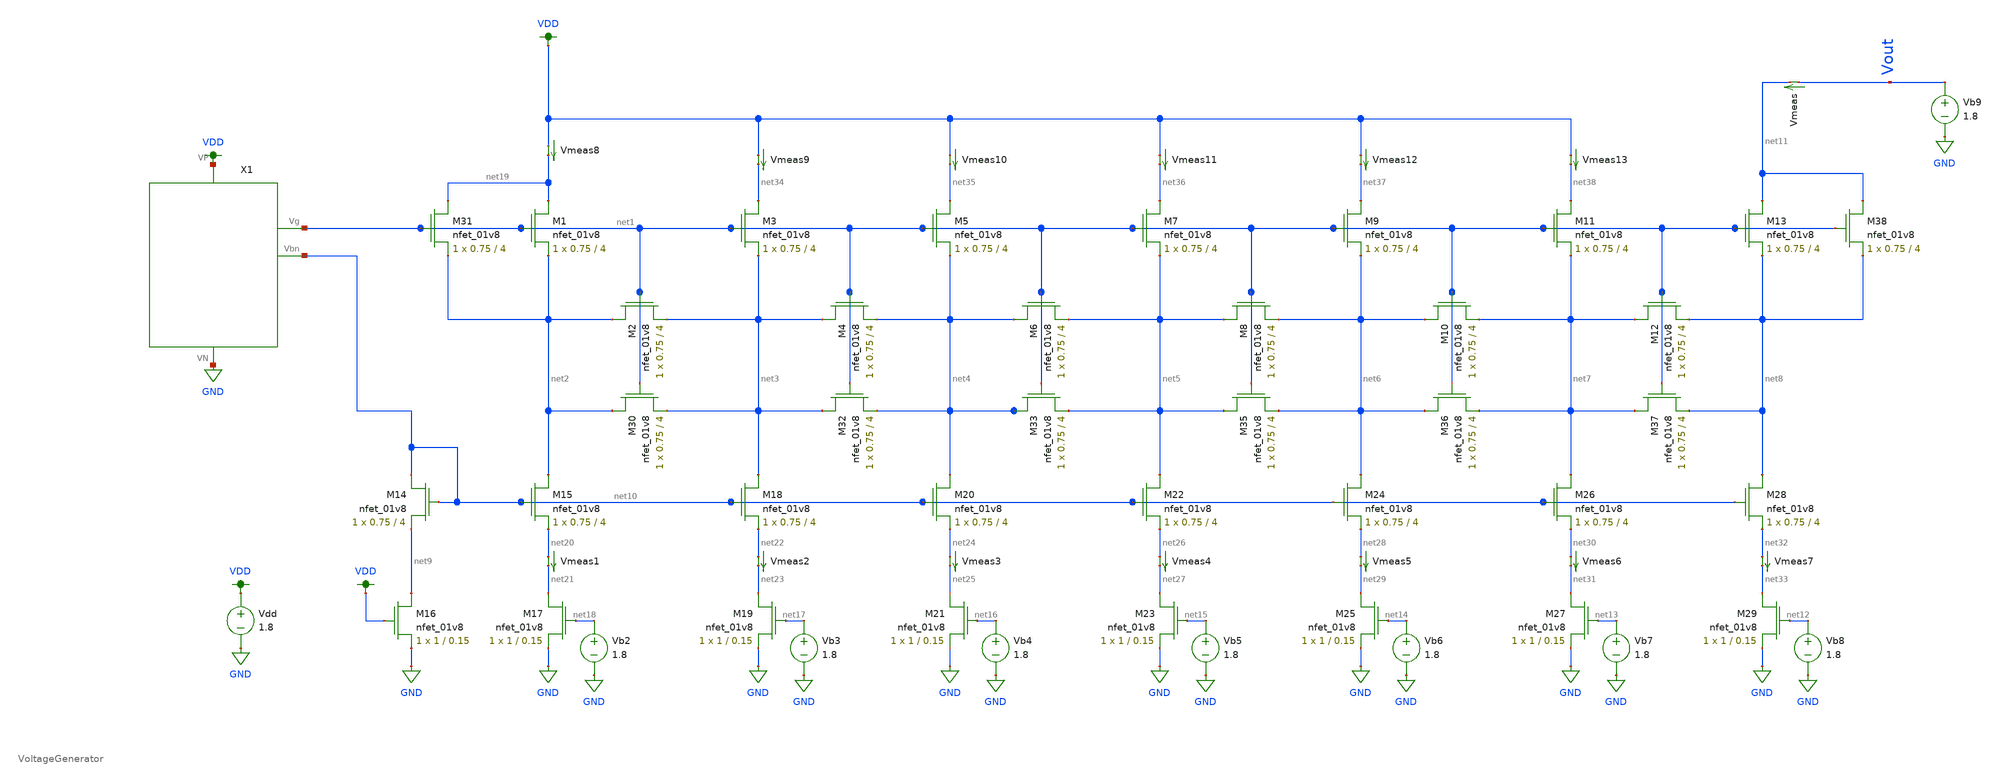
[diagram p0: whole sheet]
** sch_path: DAC_sch_test.sch
**.subckt DAC_sch_test
XM1 net19 net1 net2 GND sky130_fd_pr__nfet_01v8 L=4 W=0.75 nf=1 ad='int((nf+1)/2) * W/nf * 0.29' as='int((nf+2)/2) * W/nf * 0.29'
+ pd='2*int((nf+1)/2) * (W/nf + 0.29)' ps='2*int((nf+2)/2) * (W/nf + 0.29)' nrd='0.29 / W' nrs='0.29 / W'
+ sa=0 sb=0 sd=0 mult=1 m=1
XM2 net2 net1 net3 GND sky130_fd_pr__nfet_01v8 L=4 W=0.75 nf=1 ad='int((nf+1)/2) * W/nf * 0.29' as='int((nf+2)/2) * W/nf * 0.29'
+ pd='2*int((nf+1)/2) * (W/nf + 0.29)' ps='2*int((nf+2)/2) * (W/nf + 0.29)' nrd='0.29 / W' nrs='0.29 / W'
+ sa=0 sb=0 sd=0 mult=1 m=1
XM3 net34 net1 net3 GND sky130_fd_pr__nfet_01v8 L=4 W=0.75 nf=1 ad='int((nf+1)/2) * W/nf * 0.29' as='int((nf+2)/2) * W/nf * 0.29'
+ pd='2*int((nf+1)/2) * (W/nf + 0.29)' ps='2*int((nf+2)/2) * (W/nf + 0.29)' nrd='0.29 / W' nrs='0.29 / W'
+ sa=0 sb=0 sd=0 mult=1 m=1
XM4 net3 net1 net4 GND sky130_fd_pr__nfet_01v8 L=4 W=0.75 nf=1 ad='int((nf+1)/2) * W/nf * 0.29' as='int((nf+2)/2) * W/nf * 0.29'
+ pd='2*int((nf+1)/2) * (W/nf + 0.29)' ps='2*int((nf+2)/2) * (W/nf + 0.29)' nrd='0.29 / W' nrs='0.29 / W'
+ sa=0 sb=0 sd=0 mult=1 m=1
XM5 net35 net1 net4 GND sky130_fd_pr__nfet_01v8 L=4 W=0.75 nf=1 ad='int((nf+1)/2) * W/nf * 0.29' as='int((nf+2)/2) * W/nf * 0.29'
+ pd='2*int((nf+1)/2) * (W/nf + 0.29)' ps='2*int((nf+2)/2) * (W/nf + 0.29)' nrd='0.29 / W' nrs='0.29 / W'
+ sa=0 sb=0 sd=0 mult=1 m=1
XM6 net4 net1 net5 GND sky130_fd_pr__nfet_01v8 L=4 W=0.75 nf=1 ad='int((nf+1)/2) * W/nf * 0.29' as='int((nf+2)/2) * W/nf * 0.29'
+ pd='2*int((nf+1)/2) * (W/nf + 0.29)' ps='2*int((nf+2)/2) * (W/nf + 0.29)' nrd='0.29 / W' nrs='0.29 / W'
+ sa=0 sb=0 sd=0 mult=1 m=1
XM7 net36 net1 net5 GND sky130_fd_pr__nfet_01v8 L=4 W=0.75 nf=1 ad='int((nf+1)/2) * W/nf * 0.29' as='int((nf+2)/2) * W/nf * 0.29'
+ pd='2*int((nf+1)/2) * (W/nf + 0.29)' ps='2*int((nf+2)/2) * (W/nf + 0.29)' nrd='0.29 / W' nrs='0.29 / W'
+ sa=0 sb=0 sd=0 mult=1 m=1
XM8 net5 net1 net6 GND sky130_fd_pr__nfet_01v8 L=4 W=0.75 nf=1 ad='int((nf+1)/2) * W/nf * 0.29' as='int((nf+2)/2) * W/nf * 0.29'
+ pd='2*int((nf+1)/2) * (W/nf + 0.29)' ps='2*int((nf+2)/2) * (W/nf + 0.29)' nrd='0.29 / W' nrs='0.29 / W'
+ sa=0 sb=0 sd=0 mult=1 m=1
XM9 net37 net1 net6 GND sky130_fd_pr__nfet_01v8 L=4 W=0.75 nf=1 ad='int((nf+1)/2) * W/nf * 0.29' as='int((nf+2)/2) * W/nf * 0.29'
+ pd='2*int((nf+1)/2) * (W/nf + 0.29)' ps='2*int((nf+2)/2) * (W/nf + 0.29)' nrd='0.29 / W' nrs='0.29 / W'
+ sa=0 sb=0 sd=0 mult=1 m=1
XM10 net6 net1 net7 GND sky130_fd_pr__nfet_01v8 L=4 W=0.75 nf=1 ad='int((nf+1)/2) * W/nf * 0.29' as='int((nf+2)/2) * W/nf * 0.29'
+ pd='2*int((nf+1)/2) * (W/nf + 0.29)' ps='2*int((nf+2)/2) * (W/nf + 0.29)' nrd='0.29 / W' nrs='0.29 / W'
+ sa=0 sb=0 sd=0 mult=1 m=1
XM11 net38 net1 net7 GND sky130_fd_pr__nfet_01v8 L=4 W=0.75 nf=1 ad='int((nf+1)/2) * W/nf * 0.29' as='int((nf+2)/2) * W/nf * 0.29'
+ pd='2*int((nf+1)/2) * (W/nf + 0.29)' ps='2*int((nf+2)/2) * (W/nf + 0.29)' nrd='0.29 / W' nrs='0.29 / W'
+ sa=0 sb=0 sd=0 mult=1 m=1
XM12 net7 net1 net8 GND sky130_fd_pr__nfet_01v8 L=4 W=0.75 nf=1 ad='int((nf+1)/2) * W/nf * 0.29' as='int((nf+2)/2) * W/nf * 0.29'
+ pd='2*int((nf+1)/2) * (W/nf + 0.29)' ps='2*int((nf+2)/2) * (W/nf + 0.29)' nrd='0.29 / W' nrs='0.29 / W'
+ sa=0 sb=0 sd=0 mult=1 m=1
XM13 net11 net1 net8 GND sky130_fd_pr__nfet_01v8 L=4 W=0.75 nf=1 ad='int((nf+1)/2) * W/nf * 0.29' as='int((nf+2)/2) * W/nf * 0.29'
+ pd='2*int((nf+1)/2) * (W/nf + 0.29)' ps='2*int((nf+2)/2) * (W/nf + 0.29)' nrd='0.29 / W' nrs='0.29 / W'
+ sa=0 sb=0 sd=0 mult=1 m=1
XM14 net10 net10 net9 GND sky130_fd_pr__nfet_01v8 L=4 W=0.75 nf=1 ad='int((nf+1)/2) * W/nf * 0.29' as='int((nf+2)/2) * W/nf * 0.29'
+ pd='2*int((nf+1)/2) * (W/nf + 0.29)' ps='2*int((nf+2)/2) * (W/nf + 0.29)' nrd='0.29 / W' nrs='0.29 / W'
+ sa=0 sb=0 sd=0 mult=1 m=1
XM15 net2 net10 net20 GND sky130_fd_pr__nfet_01v8 L=4 W=0.75 nf=1 ad='int((nf+1)/2) * W/nf * 0.29' as='int((nf+2)/2) * W/nf * 0.29'
+ pd='2*int((nf+1)/2) * (W/nf + 0.29)' ps='2*int((nf+2)/2) * (W/nf + 0.29)' nrd='0.29 / W' nrs='0.29 / W'
+ sa=0 sb=0 sd=0 mult=1 m=1
XM16 net9 VDD GND GND sky130_fd_pr__nfet_01v8 L=0.15 W=1 nf=1 ad='int((nf+1)/2) * W/nf * 0.29' as='int((nf+2)/2) * W/nf * 0.29'
+ pd='2*int((nf+1)/2) * (W/nf + 0.29)' ps='2*int((nf+2)/2) * (W/nf + 0.29)' nrd='0.29 / W' nrs='0.29 / W'
+ sa=0 sb=0 sd=0 mult=1 m=1
XM17 net21 net18 GND GND sky130_fd_pr__nfet_01v8 L=0.15 W=1 nf=1 ad='int((nf+1)/2) * W/nf * 0.29' as='int((nf+2)/2) * W/nf * 0.29'
+ pd='2*int((nf+1)/2) * (W/nf + 0.29)' ps='2*int((nf+2)/2) * (W/nf + 0.29)' nrd='0.29 / W' nrs='0.29 / W'
+ sa=0 sb=0 sd=0 mult=1 m=1
XM18 net3 net10 net22 GND sky130_fd_pr__nfet_01v8 L=4 W=0.75 nf=1 ad='int((nf+1)/2) * W/nf * 0.29' as='int((nf+2)/2) * W/nf * 0.29'
+ pd='2*int((nf+1)/2) * (W/nf + 0.29)' ps='2*int((nf+2)/2) * (W/nf + 0.29)' nrd='0.29 / W' nrs='0.29 / W'
+ sa=0 sb=0 sd=0 mult=1 m=1
XM19 net23 net17 GND GND sky130_fd_pr__nfet_01v8 L=0.15 W=1 nf=1 ad='int((nf+1)/2) * W/nf * 0.29' as='int((nf+2)/2) * W/nf * 0.29'
+ pd='2*int((nf+1)/2) * (W/nf + 0.29)' ps='2*int((nf+2)/2) * (W/nf + 0.29)' nrd='0.29 / W' nrs='0.29 / W'
+ sa=0 sb=0 sd=0 mult=1 m=1
XM20 net4 net10 net24 GND sky130_fd_pr__nfet_01v8 L=4 W=0.75 nf=1 ad='int((nf+1)/2) * W/nf * 0.29' as='int((nf+2)/2) * W/nf * 0.29'
+ pd='2*int((nf+1)/2) * (W/nf + 0.29)' ps='2*int((nf+2)/2) * (W/nf + 0.29)' nrd='0.29 / W' nrs='0.29 / W'
+ sa=0 sb=0 sd=0 mult=1 m=1
XM21 net25 net16 GND GND sky130_fd_pr__nfet_01v8 L=0.15 W=1 nf=1 ad='int((nf+1)/2) * W/nf * 0.29' as='int((nf+2)/2) * W/nf * 0.29'
+ pd='2*int((nf+1)/2) * (W/nf + 0.29)' ps='2*int((nf+2)/2) * (W/nf + 0.29)' nrd='0.29 / W' nrs='0.29 / W'
+ sa=0 sb=0 sd=0 mult=1 m=1
XM22 net5 net10 net26 GND sky130_fd_pr__nfet_01v8 L=4 W=0.75 nf=1 ad='int((nf+1)/2) * W/nf * 0.29' as='int((nf+2)/2) * W/nf * 0.29'
+ pd='2*int((nf+1)/2) * (W/nf + 0.29)' ps='2*int((nf+2)/2) * (W/nf + 0.29)' nrd='0.29 / W' nrs='0.29 / W'
+ sa=0 sb=0 sd=0 mult=1 m=1
XM23 net27 net15 GND GND sky130_fd_pr__nfet_01v8 L=0.15 W=1 nf=1 ad='int((nf+1)/2) * W/nf * 0.29' as='int((nf+2)/2) * W/nf * 0.29'
+ pd='2*int((nf+1)/2) * (W/nf + 0.29)' ps='2*int((nf+2)/2) * (W/nf + 0.29)' nrd='0.29 / W' nrs='0.29 / W'
+ sa=0 sb=0 sd=0 mult=1 m=1
XM24 net6 net10 net28 GND sky130_fd_pr__nfet_01v8 L=4 W=0.75 nf=1 ad='int((nf+1)/2) * W/nf * 0.29' as='int((nf+2)/2) * W/nf * 0.29'
+ pd='2*int((nf+1)/2) * (W/nf + 0.29)' ps='2*int((nf+2)/2) * (W/nf + 0.29)' nrd='0.29 / W' nrs='0.29 / W'
+ sa=0 sb=0 sd=0 mult=1 m=1
XM25 net29 net14 GND GND sky130_fd_pr__nfet_01v8 L=0.15 W=1 nf=1 ad='int((nf+1)/2) * W/nf * 0.29' as='int((nf+2)/2) * W/nf * 0.29'
+ pd='2*int((nf+1)/2) * (W/nf + 0.29)' ps='2*int((nf+2)/2) * (W/nf + 0.29)' nrd='0.29 / W' nrs='0.29 / W'
+ sa=0 sb=0 sd=0 mult=1 m=1
XM26 net7 net10 net30 GND sky130_fd_pr__nfet_01v8 L=4 W=0.75 nf=1 ad='int((nf+1)/2) * W/nf * 0.29' as='int((nf+2)/2) * W/nf * 0.29'
+ pd='2*int((nf+1)/2) * (W/nf + 0.29)' ps='2*int((nf+2)/2) * (W/nf + 0.29)' nrd='0.29 / W' nrs='0.29 / W'
+ sa=0 sb=0 sd=0 mult=1 m=1
XM27 net31 net13 GND GND sky130_fd_pr__nfet_01v8 L=0.15 W=1 nf=1 ad='int((nf+1)/2) * W/nf * 0.29' as='int((nf+2)/2) * W/nf * 0.29'
+ pd='2*int((nf+1)/2) * (W/nf + 0.29)' ps='2*int((nf+2)/2) * (W/nf + 0.29)' nrd='0.29 / W' nrs='0.29 / W'
+ sa=0 sb=0 sd=0 mult=1 m=1
XM28 net8 net10 net32 GND sky130_fd_pr__nfet_01v8 L=4 W=0.75 nf=1 ad='int((nf+1)/2) * W/nf * 0.29' as='int((nf+2)/2) * W/nf * 0.29'
+ pd='2*int((nf+1)/2) * (W/nf + 0.29)' ps='2*int((nf+2)/2) * (W/nf + 0.29)' nrd='0.29 / W' nrs='0.29 / W'
+ sa=0 sb=0 sd=0 mult=1 m=1
XM29 net33 net12 GND GND sky130_fd_pr__nfet_01v8 L=0.15 W=1 nf=1 ad='int((nf+1)/2) * W/nf * 0.29' as='int((nf+2)/2) * W/nf * 0.29'
+ pd='2*int((nf+1)/2) * (W/nf + 0.29)' ps='2*int((nf+2)/2) * (W/nf + 0.29)' nrd='0.29 / W' nrs='0.29 / W'
+ sa=0 sb=0 sd=0 mult=1 m=1
XM30 net2 net1 net3 GND sky130_fd_pr__nfet_01v8 L=4 W=0.75 nf=1 ad='int((nf+1)/2) * W/nf * 0.29' as='int((nf+2)/2) * W/nf * 0.29'
+ pd='2*int((nf+1)/2) * (W/nf + 0.29)' ps='2*int((nf+2)/2) * (W/nf + 0.29)' nrd='0.29 / W' nrs='0.29 / W'
+ sa=0 sb=0 sd=0 mult=1 m=1
XM31 net19 net1 net2 GND sky130_fd_pr__nfet_01v8 L=4 W=0.75 nf=1 ad='int((nf+1)/2) * W/nf * 0.29' as='int((nf+2)/2) * W/nf * 0.29'
+ pd='2*int((nf+1)/2) * (W/nf + 0.29)' ps='2*int((nf+2)/2) * (W/nf + 0.29)' nrd='0.29 / W' nrs='0.29 / W'
+ sa=0 sb=0 sd=0 mult=1 m=1
XM32 net3 net1 net4 GND sky130_fd_pr__nfet_01v8 L=4 W=0.75 nf=1 ad='int((nf+1)/2) * W/nf * 0.29' as='int((nf+2)/2) * W/nf * 0.29'
+ pd='2*int((nf+1)/2) * (W/nf + 0.29)' ps='2*int((nf+2)/2) * (W/nf + 0.29)' nrd='0.29 / W' nrs='0.29 / W'
+ sa=0 sb=0 sd=0 mult=1 m=1
XM33 net4 net1 net5 GND sky130_fd_pr__nfet_01v8 L=4 W=0.75 nf=1 ad='int((nf+1)/2) * W/nf * 0.29' as='int((nf+2)/2) * W/nf * 0.29'
+ pd='2*int((nf+1)/2) * (W/nf + 0.29)' ps='2*int((nf+2)/2) * (W/nf + 0.29)' nrd='0.29 / W' nrs='0.29 / W'
+ sa=0 sb=0 sd=0 mult=1 m=1
XM35 net5 net1 net6 GND sky130_fd_pr__nfet_01v8 L=4 W=0.75 nf=1 ad='int((nf+1)/2) * W/nf * 0.29' as='int((nf+2)/2) * W/nf * 0.29'
+ pd='2*int((nf+1)/2) * (W/nf + 0.29)' ps='2*int((nf+2)/2) * (W/nf + 0.29)' nrd='0.29 / W' nrs='0.29 / W'
+ sa=0 sb=0 sd=0 mult=1 m=1
XM36 net6 net1 net7 GND sky130_fd_pr__nfet_01v8 L=4 W=0.75 nf=1 ad='int((nf+1)/2) * W/nf * 0.29' as='int((nf+2)/2) * W/nf * 0.29'
+ pd='2*int((nf+1)/2) * (W/nf + 0.29)' ps='2*int((nf+2)/2) * (W/nf + 0.29)' nrd='0.29 / W' nrs='0.29 / W'
+ sa=0 sb=0 sd=0 mult=1 m=1
XM37 net7 net1 net8 GND sky130_fd_pr__nfet_01v8 L=4 W=0.75 nf=1 ad='int((nf+1)/2) * W/nf * 0.29' as='int((nf+2)/2) * W/nf * 0.29'
+ pd='2*int((nf+1)/2) * (W/nf + 0.29)' ps='2*int((nf+2)/2) * (W/nf + 0.29)' nrd='0.29 / W' nrs='0.29 / W'
+ sa=0 sb=0 sd=0 mult=1 m=1
XM38 net11 net1 net8 GND sky130_fd_pr__nfet_01v8 L=4 W=0.75 nf=1 ad='int((nf+1)/2) * W/nf * 0.29' as='int((nf+2)/2) * W/nf * 0.29'
+ pd='2*int((nf+1)/2) * (W/nf + 0.29)' ps='2*int((nf+2)/2) * (W/nf + 0.29)' nrd='0.29 / W' nrs='0.29 / W'
+ sa=0 sb=0 sd=0 mult=1 m=1
X1 GND VDD net1 net10 VoltageGenerator
Vmeas Vout net11 0
.save i(vmeas)
Vb2 net18 GND 1.8
Vb3 net17 GND 1.8
Vb4 net16 GND 1.8
Vb5 net15 GND 1.8
Vb6 net14 GND 1.8
Vb7 net13 GND 1.8
Vb8 net12 GND 1.8
Vdd VDD GND 1.8
Vb9 Vout GND 1.8
Vmeas1 net20 net21 0
.save i(vmeas1)
Vmeas2 net22 net23 0
.save i(vmeas2)
Vmeas3 net24 net25 0
.save i(vmeas3)
Vmeas4 net26 net27 0
.save i(vmeas4)
Vmeas5 net28 net29 0
.save i(vmeas5)
Vmeas6 net30 net31 0
.save i(vmeas6)
Vmeas7 net32 net33 0
.save i(vmeas7)
Vmeas8 VDD net19 0
.save i(vmeas8)
Vmeas9 VDD net34 0
.save i(vmeas9)
Vmeas10 VDD net35 0
.save i(vmeas10)
Vmeas11 VDD net36 0
.save i(vmeas11)
Vmeas12 VDD net37 0
.save i(vmeas12)
Vmeas13 VDD net38 0
.save i(vmeas13)
**** begin user architecture code

.control
set wr_vecnames
set wr_singlescale

let mc_runs = 10
let run = 1
dowhile run <= mc_runs
dc vb2 0 1.8 0.01
wrdata ~/Documents/mctut/mp4{$&run}.txt v(Vout)
reset
let run = run + 1
end
.endcname=s1


.option wnflag=1
.param MC_SWITCH=0.0
.lib ~/skywater/skywater-pdk/libraries/sky130_fd_pr_ngspice/latest/models/sky130.lib.spice tt

**** end user architecture code
**.ends
.GLOBAL GND
.GLOBAL VDD
.end
